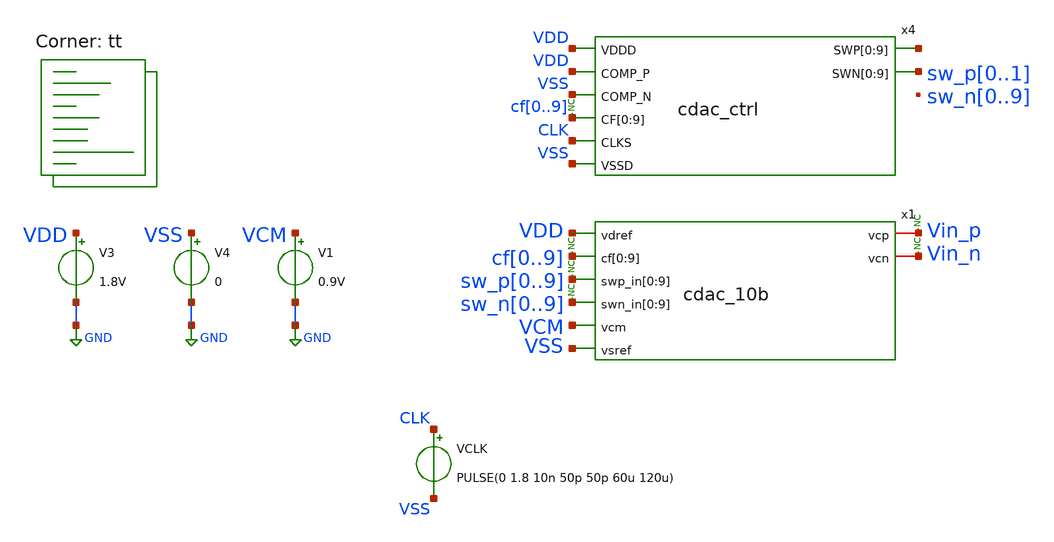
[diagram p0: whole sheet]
** sch_path: xschem/untitled-1.sch
**.subckt untitled-1
V3 VDD GND 1.8V
V4 VSS GND 0
* noconn Vin_p
* noconn Vin_n
* noconn cf[0..9]
x1 VDD cf0 cf1 cf2 cf3 cf4 cf5 cf6 cf7 cf8 cf9 sw_p0 sw_p1 sw_p2 sw_p3 sw_p4 sw_p5 sw_p6 sw_p7 sw_p8
+ sw_p9 sw_n0 sw_n1 sw_n2 sw_n3 sw_n4 sw_n5 sw_n6 sw_n7 sw_n8 sw_n9 VCM VSS Vin_p Vin_n cdac_10b
V1 VCM GND 0.9V
* noconn sw_p[0..9]
* noconn sw_n[0..9]
x4 VDD VDD VSS cf0 cf1 cf2 cf3 cf4 cf5 cf6 cf7 cf8 cf9 CLK VSS net1[9] net1[8] net1[7] net1[6]
+ net1[5] net1[4] net1[3] net1[2] net1[1] net1[0] sw_p0 sw_p1 sw_p0 sw_p1 sw_p0 sw_p1 sw_p0 sw_p1 sw_p0 sw_p1
+ cdac_ctrl
* noconn cf[0..9]
VCLK CLK VSS PULSE(0 1.8 10n 50p 50p 60u 120u)
**** begin user architecture code
 *.lib $::SKYWATER_MODELS/sky130.lib.spice tt
.include $::SKYWATER_STDCELLS/sky130_fd_sc_hd.spice


.options acct list
.temp 25
*vvcc VDD 0 dc 1.8
*vvss VSS 0 0

v_sp_f1 cf0 gnd  PULSE(1.8V 0 0 1ns 1ns 5us 200us)
v_sp_f2 cf1 gnd  PULSE(1.8V 0 0 1ns 1ns 10us 200us)
v_sp_f3 cf2 gnd  PULSE(1.8V 0 0 1ns 1ns 15us 200us)
v_sp_f4 cf3 gnd  PULSE(1.8V 0 0 1ns 1ns 20us 200us)
v_sp_f5 cf4 gnd  PULSE(1.8V 0 0 1ns 1ns 25us 200us)
v_sp_f6 cf5 gnd  PULSE(1.8V 0 0 1ns 1ns 30us 200us)
v_sp_f7 cf6 gnd  PULSE(1.8V 0 0 1ns 1ns 35us 200us)
v_sp_f8 cf7 gnd  PULSE(1.8V 0 0 1ns 1ns 45us 200us)
v_sp_f9 cf8 gnd  PULSE(1.8V 0 0 1ns 1ns 50us 200us)
v_sp_f10 cf9 gnd  PULSE(1.8V 0 0 1ns 1ns 55us 200us)

.control
ic v(vin_p)=0.9V
ic v(vin_n)=0.9V
save all
tran 0.1u 110u
write untitled-1.raw
plot Vin_n Vin_p+2
.endc


.lib $::SKYWATER_MODELS/sky130.lib.spice tt
**** end user architecture code
**.ends
.GLOBAL GND
.end
